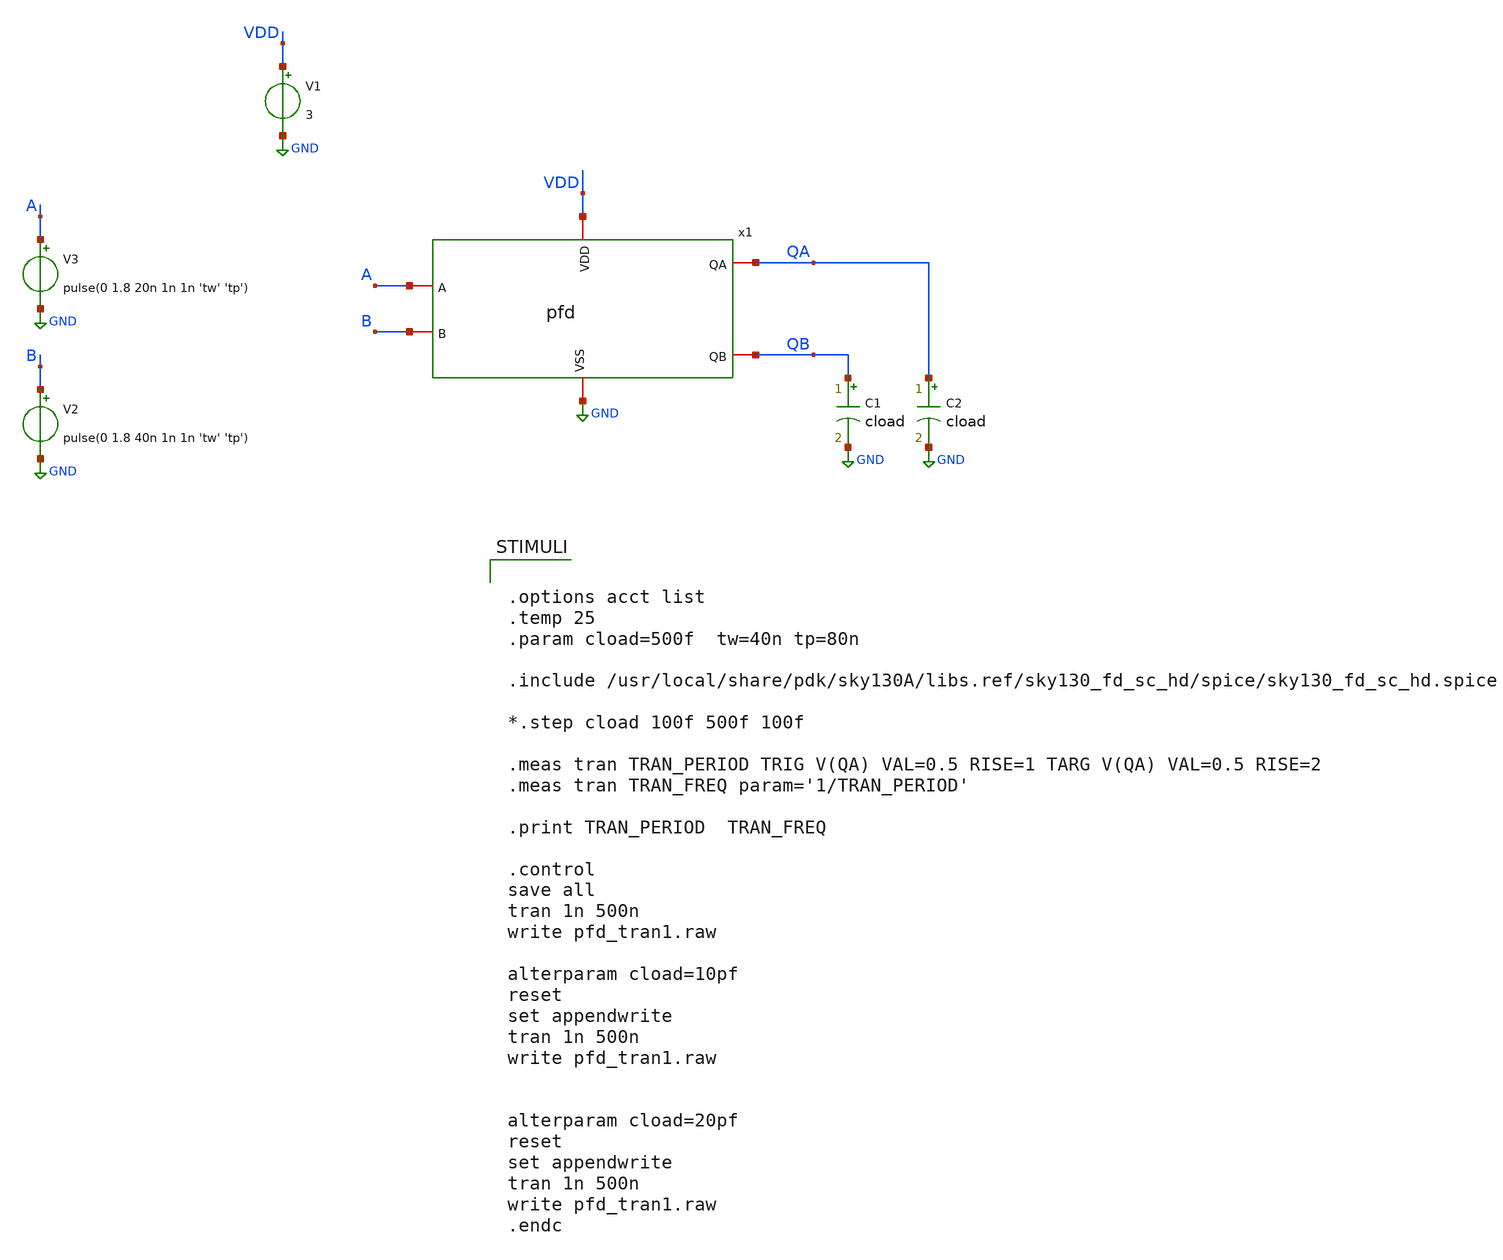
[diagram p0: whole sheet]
** sch_path: xschem01/pfd/pfd_tran1.sch
**.subckt pfd_tran1
x1 GND VDD A QA QB B pfd
V1 VDD GND 3
V2 B GND pulse(0 1.8 40n 1n 1n 'tw' 'tp')
V3 A GND pulse(0 1.8 20n 1n 1n 'tw' 'tp')
C1 QB GND cload m=1
C2 QA GND cload m=1
**** begin user architecture code


.options acct list
.temp 25
.param cload=500f  tw=40n tp=80n

.include /usr/local/share/pdk/sky130A/libs.ref/sky130_fd_sc_hd/spice/sky130_fd_sc_hd.spice

*.step cload 100f 500f 100f

.meas tran TRAN_PERIOD TRIG V(QA) VAL=0.5 RISE=1 TARG V(QA) VAL=0.5 RISE=2
.meas tran TRAN_FREQ param='1/TRAN_PERIOD'

.print TRAN_PERIOD  TRAN_FREQ

.control
save all
tran 1n 500n
write pfd_tran1.raw

alterparam cload=10pf
reset
set appendwrite
tran 1n 500n
write pfd_tran1.raw


alterparam cload=20pf
reset
set appendwrite
tran 1n 500n
write pfd_tran1.raw
.endc



** opencircuitdesign pdks install
.lib $::SKYWATER_MODELS/sky130.lib.spice tt


**** end user architecture code
**.ends
.GLOBAL GND
.end
